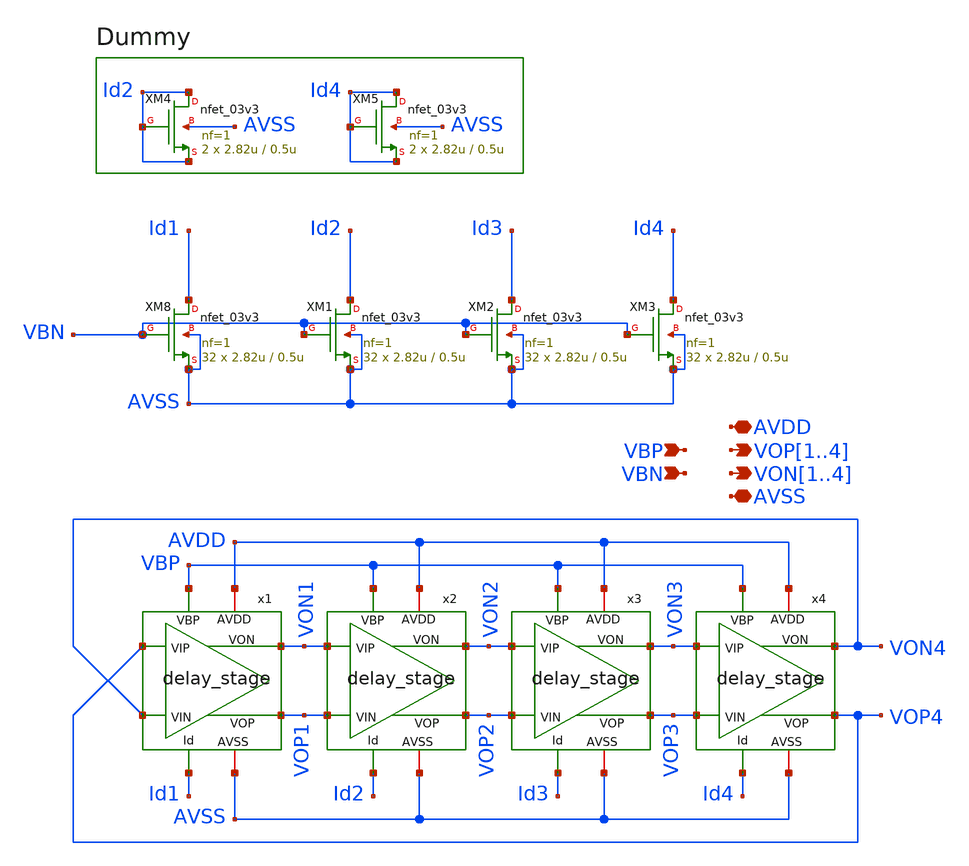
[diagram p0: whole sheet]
** sch_path: designs/libs/core_analog/vco/vco.sch
**.subckt vco VOP1,VOP2,VOP3,VOP4 VON1,VON2,VON3,VON4 VBP VBN AVDD AVSS
*.opin VOP1,VOP2,VOP3,VOP4
*.opin VON1,VON2,VON3,VON4
*.ipin VBP
*.ipin VBN
*.iopin AVDD
*.iopin AVSS
x1 VOP1 AVDD VOP4 VON4 VON1 AVSS VBP Id1 delay_stage
x2 VOP2 AVDD VON1 VOP1 VON2 AVSS VBP Id2 delay_stage
x3 VOP3 AVDD VON2 VOP2 VON3 AVSS VBP Id3 delay_stage
x4 VOP4 AVDD VON3 VOP3 VON4 AVSS VBP Id4 delay_stage
XM8 Id1 VBN AVSS AVSS nfet_03v3 L=0.5u W=2.82u nf=1 ad='int((nf+1)/2) * W/nf * 0.18u' as='int((nf+2)/2) * W/nf * 0.18u'
+ pd='2*int((nf+1)/2) * (W/nf + 0.18u)' ps='2*int((nf+2)/2) * (W/nf + 0.18u)' nrd='0.18u / W' nrs='0.18u / W'
+ sa=0 sb=0 sd=0 m=32
XM1 Id2 VBN AVSS AVSS nfet_03v3 L=0.5u W=2.82u nf=1 ad='int((nf+1)/2) * W/nf * 0.18u' as='int((nf+2)/2) * W/nf * 0.18u'
+ pd='2*int((nf+1)/2) * (W/nf + 0.18u)' ps='2*int((nf+2)/2) * (W/nf + 0.18u)' nrd='0.18u / W' nrs='0.18u / W'
+ sa=0 sb=0 sd=0 m=32
XM2 Id3 VBN AVSS AVSS nfet_03v3 L=0.5u W=2.82u nf=1 ad='int((nf+1)/2) * W/nf * 0.18u' as='int((nf+2)/2) * W/nf * 0.18u'
+ pd='2*int((nf+1)/2) * (W/nf + 0.18u)' ps='2*int((nf+2)/2) * (W/nf + 0.18u)' nrd='0.18u / W' nrs='0.18u / W'
+ sa=0 sb=0 sd=0 m=32
XM3 Id4 VBN AVSS AVSS nfet_03v3 L=0.5u W=2.82u nf=1 ad='int((nf+1)/2) * W/nf * 0.18u' as='int((nf+2)/2) * W/nf * 0.18u'
+ pd='2*int((nf+1)/2) * (W/nf + 0.18u)' ps='2*int((nf+2)/2) * (W/nf + 0.18u)' nrd='0.18u / W' nrs='0.18u / W'
+ sa=0 sb=0 sd=0 m=32
XM4 Id2 Id2 Id2 AVSS nfet_03v3 L=0.5u W=2.82u nf=1 ad='int((nf+1)/2) * W/nf * 0.18u' as='int((nf+2)/2) * W/nf * 0.18u'
+ pd='2*int((nf+1)/2) * (W/nf + 0.18u)' ps='2*int((nf+2)/2) * (W/nf + 0.18u)' nrd='0.18u / W' nrs='0.18u / W'
+ sa=0 sb=0 sd=0 m=2
XM5 Id4 Id4 Id4 AVSS nfet_03v3 L=0.5u W=2.82u nf=1 ad='int((nf+1)/2) * W/nf * 0.18u' as='int((nf+2)/2) * W/nf * 0.18u'
+ pd='2*int((nf+1)/2) * (W/nf + 0.18u)' ps='2*int((nf+2)/2) * (W/nf + 0.18u)' nrd='0.18u / W' nrs='0.18u / W'
+ sa=0 sb=0 sd=0 m=2
**.ends

* expanding   symbol:  libs/core_analog/delay_stage/delay_stage.sym # of pins=8
** sym_path: designs/libs/core_analog/delay_stage/delay_stage.sym
** sch_path: designs/libs/core_analog/delay_stage/delay_stage.sch
.subckt delay_stage VOP AVDD VIP VIN VON AVSS VBP Id
*.ipin VIP
*.ipin VIN
*.opin VOP
*.opin VON
*.iopin AVDD
*.iopin AVSS
*.ipin VBP
*.ipin Id
XM5 VON VIP Id AVSS nfet_03v3 L=0.5u W=2.08u nf=1 ad='int((nf+1)/2) * W/nf * 0.18u' as='int((nf+2)/2) * W/nf * 0.18u'
+ pd='2*int((nf+1)/2) * (W/nf + 0.18u)' ps='2*int((nf+2)/2) * (W/nf + 0.18u)' nrd='0.18u / W' nrs='0.18u / W'
+ sa=0 sb=0 sd=0 m=8
XM2 VON VON AVDD AVDD pfet_03v3 L=1.5u W=1.1u nf=1 ad='int((nf+1)/2) * W/nf * 0.18u' as='int((nf+2)/2) * W/nf * 0.18u'
+ pd='2*int((nf+1)/2) * (W/nf + 0.18u)' ps='2*int((nf+2)/2) * (W/nf + 0.18u)' nrd='0.18u / W' nrs='0.18u / W'
+ sa=0 sb=0 sd=0 m=8
XM6 VOP VIN Id AVSS nfet_03v3 L=0.5u W=2.08u nf=1 ad='int((nf+1)/2) * W/nf * 0.18u' as='int((nf+2)/2) * W/nf * 0.18u'
+ pd='2*int((nf+1)/2) * (W/nf + 0.18u)' ps='2*int((nf+2)/2) * (W/nf + 0.18u)' nrd='0.18u / W' nrs='0.18u / W'
+ sa=0 sb=0 sd=0 m=8
XM1 VON VBP AVDD AVDD pfet_03v3 L=1.5u W=1.1u nf=1 ad='int((nf+1)/2) * W/nf * 0.18u' as='int((nf+2)/2) * W/nf * 0.18u'
+ pd='2*int((nf+1)/2) * (W/nf + 0.18u)' ps='2*int((nf+2)/2) * (W/nf + 0.18u)' nrd='0.18u / W' nrs='0.18u / W'
+ sa=0 sb=0 sd=0 m=8
XM3 VOP VBP AVDD AVDD pfet_03v3 L=1.5u W=1.1u nf=1 ad='int((nf+1)/2) * W/nf * 0.18u' as='int((nf+2)/2) * W/nf * 0.18u'
+ pd='2*int((nf+1)/2) * (W/nf + 0.18u)' ps='2*int((nf+2)/2) * (W/nf + 0.18u)' nrd='0.18u / W' nrs='0.18u / W'
+ sa=0 sb=0 sd=0 m=8
XM4 VOP VOP AVDD AVDD pfet_03v3 L=1.5u W=1.1u nf=1 ad='int((nf+1)/2) * W/nf * 0.18u' as='int((nf+2)/2) * W/nf * 0.18u'
+ pd='2*int((nf+1)/2) * (W/nf + 0.18u)' ps='2*int((nf+2)/2) * (W/nf + 0.18u)' nrd='0.18u / W' nrs='0.18u / W'
+ sa=0 sb=0 sd=0 m=8
.ends

.end
